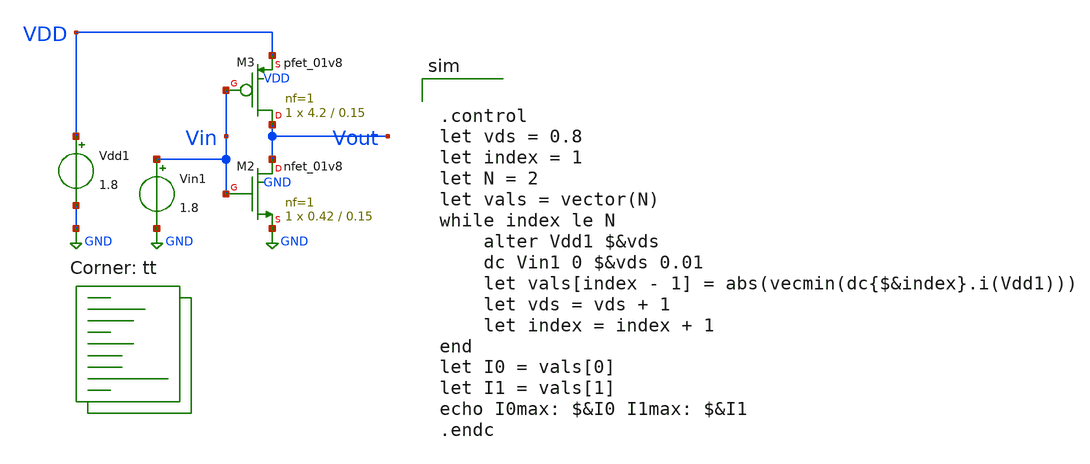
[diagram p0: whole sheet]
** sch_path: tutorial_3/tutorial_3_1d.sch
**.subckt tutorial_3_1d
XM2 Vout Vin GND GND sky130_fd_pr__nfet_01v8 L=0.15 W=0.42 nf=1 ad='int((nf+1)/2) * W/nf * 0.29' as='int((nf+2)/2) * W/nf * 0.29'
+ pd='2*int((nf+1)/2) * (W/nf + 0.29)' ps='2*int((nf+2)/2) * (W/nf + 0.29)' nrd='0.29 / W' nrs='0.29 / W'
+ sa=0 sb=0 sd=0 mult=1 m=1
XM3 Vout Vin VDD VDD sky130_fd_pr__pfet_01v8 L=0.15 W=4.2 nf=1 ad='int((nf+1)/2) * W/nf * 0.29' as='int((nf+2)/2) * W/nf * 0.29'
+ pd='2*int((nf+1)/2) * (W/nf + 0.29)' ps='2*int((nf+2)/2) * (W/nf + 0.29)' nrd='0.29 / W' nrs='0.29 / W'
+ sa=0 sb=0 sd=0 mult=1 m=1
Vin1 Vin GND 1.8
Vdd1 VDD GND 1.8
**** begin user architecture code
.lib $::SKYWATER_MODELS/sky130.lib.spice tt


.control
let vds = 0.8
let index = 1
let N = 2
let vals = vector(N)
while index le N
    alter Vdd1 $&vds
    dc Vin1 0 $&vds 0.01
    let vals[index - 1] = abs(vecmin(dc{$&index}.i(Vdd1)))
    let vds = vds + 1
    let index = index + 1
end
let I0 = vals[0]
let I1 = vals[1]
echo I0max: $&I0 I1max: $&I1
.endc

**** end user architecture code
**.ends
.GLOBAL GND
.end
